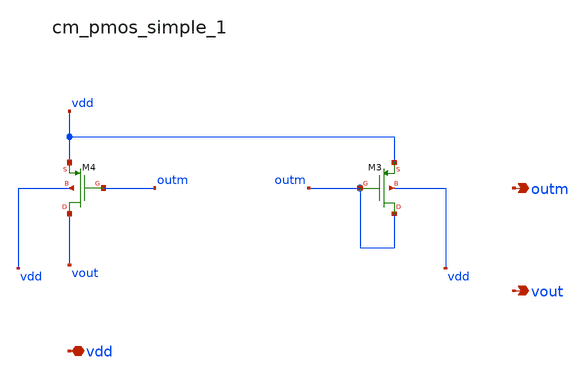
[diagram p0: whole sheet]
** sch_path: analog-db/raw/amp_001_5t/hier/blocks/cm_pmos_simple_1.sch
**.subckt cm_pmos_simple_1 vdd outm vout
*.iopin vdd
*.opin outm
*.opin vout
XM3 outm outm vdd vdd sg13_lv_pmos w=x_dut_xm3_w l=x_dut_xm3_l ng=1 m=x_dut_xm3_m
XM4 vout outm vdd vdd sg13_lv_pmos w=x_dut_xm4_w l=x_dut_xm4_l ng=1 m=x_dut_xm4_m
**.ends
.end
